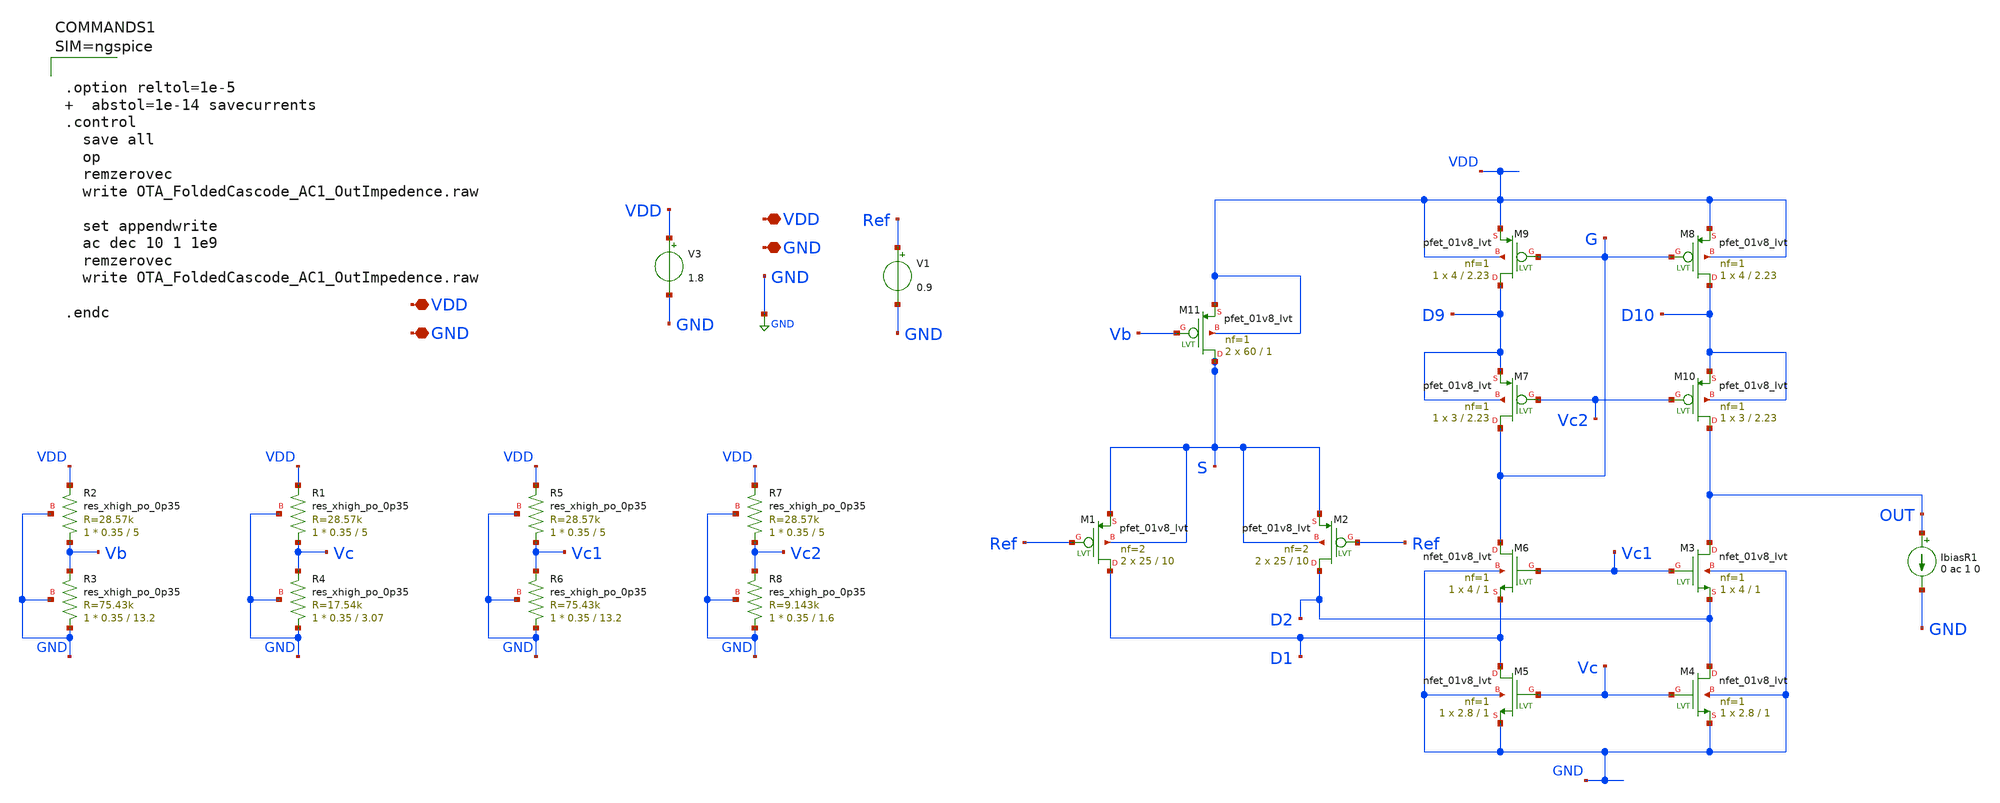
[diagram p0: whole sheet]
** sch_path: xschem/OTA_FoldedCascode_AC1_OutImpedence.sch
**.subckt OTA_FoldedCascode_AC1_OutImpedence VDD GND VDD GND
*.iopin VDD
*.iopin GND
*.iopin VDD
*.iopin GND
IbiasR1 OUT GND 0 ac 1 0
V3 VDD GND 1.8
XM11 S Vb VDD VDD sky130_fd_pr__pfet_01v8_lvt L=1 W=60 nf=1 ad='int((nf+1)/2) * W/nf * 0.29' as='int((nf+2)/2) * W/nf * 0.29'
+ pd='2*int((nf+1)/2) * (W/nf + 0.29)' ps='2*int((nf+2)/2) * (W/nf + 0.29)' nrd='0.29 / W' nrs='0.29 / W'
+ sa=0 sb=0 sd=0 mult=2 m=2
XM1 D1 Ref S S sky130_fd_pr__pfet_01v8_lvt L=10 W=25 nf=2 ad='int((nf+1)/2) * W/nf * 0.29' as='int((nf+2)/2) * W/nf * 0.29'
+ pd='2*int((nf+1)/2) * (W/nf + 0.29)' ps='2*int((nf+2)/2) * (W/nf + 0.29)' nrd='0.29 / W' nrs='0.29 / W'
+ sa=0 sb=0 sd=0 mult=2 m=2
XM2 D2 Ref S S sky130_fd_pr__pfet_01v8_lvt L=10 W=25 nf=2 ad='int((nf+1)/2) * W/nf * 0.29' as='int((nf+2)/2) * W/nf * 0.29'
+ pd='2*int((nf+1)/2) * (W/nf + 0.29)' ps='2*int((nf+2)/2) * (W/nf + 0.29)' nrd='0.29 / W' nrs='0.29 / W'
+ sa=0 sb=0 sd=0 mult=2 m=2
XM3 OUT Vc1 D2 GND sky130_fd_pr__nfet_01v8_lvt L=1 W=4 nf=1 ad='int((nf+1)/2) * W/nf * 0.29' as='int((nf+2)/2) * W/nf * 0.29'
+ pd='2*int((nf+1)/2) * (W/nf + 0.29)' ps='2*int((nf+2)/2) * (W/nf + 0.29)' nrd='0.29 / W' nrs='0.29 / W'
+ sa=0 sb=0 sd=0 mult=1 m=1
XM4 D2 Vc GND GND sky130_fd_pr__nfet_01v8_lvt L=1 W=2.8 nf=1 ad='int((nf+1)/2) * W/nf * 0.29' as='int((nf+2)/2) * W/nf * 0.29'
+ pd='2*int((nf+1)/2) * (W/nf + 0.29)' ps='2*int((nf+2)/2) * (W/nf + 0.29)' nrd='0.29 / W' nrs='0.29 / W'
+ sa=0 sb=0 sd=0 mult=1 m=1
XM5 D1 Vc GND GND sky130_fd_pr__nfet_01v8_lvt L=1 W=2.8 nf=1 ad='int((nf+1)/2) * W/nf * 0.29' as='int((nf+2)/2) * W/nf * 0.29'
+ pd='2*int((nf+1)/2) * (W/nf + 0.29)' ps='2*int((nf+2)/2) * (W/nf + 0.29)' nrd='0.29 / W' nrs='0.29 / W'
+ sa=0 sb=0 sd=0 mult=1 m=1
XM6 G Vc1 D1 GND sky130_fd_pr__nfet_01v8_lvt L=1 W=4 nf=1 ad='int((nf+1)/2) * W/nf * 0.29' as='int((nf+2)/2) * W/nf * 0.29'
+ pd='2*int((nf+1)/2) * (W/nf + 0.29)' ps='2*int((nf+2)/2) * (W/nf + 0.29)' nrd='0.29 / W' nrs='0.29 / W'
+ sa=0 sb=0 sd=0 mult=1 m=1
XM7 G Vc2 D9 D9 sky130_fd_pr__pfet_01v8_lvt L=2.23 W=3 nf=1 ad='int((nf+1)/2) * W/nf * 0.29' as='int((nf+2)/2) * W/nf * 0.29'
+ pd='2*int((nf+1)/2) * (W/nf + 0.29)' ps='2*int((nf+2)/2) * (W/nf + 0.29)' nrd='0.29 / W' nrs='0.29 / W'
+ sa=0 sb=0 sd=0 mult=1 m=1
XM9 D9 G VDD VDD sky130_fd_pr__pfet_01v8_lvt L=2.23 W=4 nf=1 ad='int((nf+1)/2) * W/nf * 0.29' as='int((nf+2)/2) * W/nf * 0.29'
+ pd='2*int((nf+1)/2) * (W/nf + 0.29)' ps='2*int((nf+2)/2) * (W/nf + 0.29)' nrd='0.29 / W' nrs='0.29 / W'
+ sa=0 sb=0 sd=0 mult=1 m=1
XM8 D10 G VDD VDD sky130_fd_pr__pfet_01v8_lvt L=2.23 W=4 nf=1 ad='int((nf+1)/2) * W/nf * 0.29' as='int((nf+2)/2) * W/nf * 0.29'
+ pd='2*int((nf+1)/2) * (W/nf + 0.29)' ps='2*int((nf+2)/2) * (W/nf + 0.29)' nrd='0.29 / W' nrs='0.29 / W'
+ sa=0 sb=0 sd=0 mult=1 m=1
XM10 OUT Vc2 D10 D10 sky130_fd_pr__pfet_01v8_lvt L=2.23 W=3 nf=1 ad='int((nf+1)/2) * W/nf * 0.29' as='int((nf+2)/2) * W/nf * 0.29'
+ pd='2*int((nf+1)/2) * (W/nf + 0.29)' ps='2*int((nf+2)/2) * (W/nf + 0.29)' nrd='0.29 / W' nrs='0.29 / W'
+ sa=0 sb=0 sd=0 mult=1 m=1
V1 Ref GND 0.9
XR2 Vb VDD GND sky130_fd_pr__res_xhigh_po_0p35 L=5 mult=1 m=1
XR3 GND Vb GND sky130_fd_pr__res_xhigh_po_0p35 L=13.2 mult=1 m=1
XR1 Vc VDD GND sky130_fd_pr__res_xhigh_po_0p35 L=5 mult=1 m=1
XR4 GND Vc GND sky130_fd_pr__res_xhigh_po_0p35 L=3.07 mult=1 m=1
XR5 Vc1 VDD GND sky130_fd_pr__res_xhigh_po_0p35 L=5 mult=1 m=1
XR6 GND Vc1 GND sky130_fd_pr__res_xhigh_po_0p35 L=13.2 mult=1 m=1
XR7 Vc2 VDD GND sky130_fd_pr__res_xhigh_po_0p35 L=5 mult=1 m=1
XR8 GND Vc2 GND sky130_fd_pr__res_xhigh_po_0p35 L=1.6 mult=1 m=1
**** begin user architecture code



.option reltol=1e-5   abstol=1e-14 savecurrents
.control
  save all
  op
  remzerovec
  write OTA_FoldedCascode_AC1_OutImpedence.raw

  set appendwrite
  ac dec 10 1 1e9
  remzerovec
  write OTA_FoldedCascode_AC1_OutImpedence.raw

.endc



.lib $::SKYWATER_MODELS/sky130.lib.spice tt
**** end user architecture code
**.ends
.GLOBAL GND
.end
